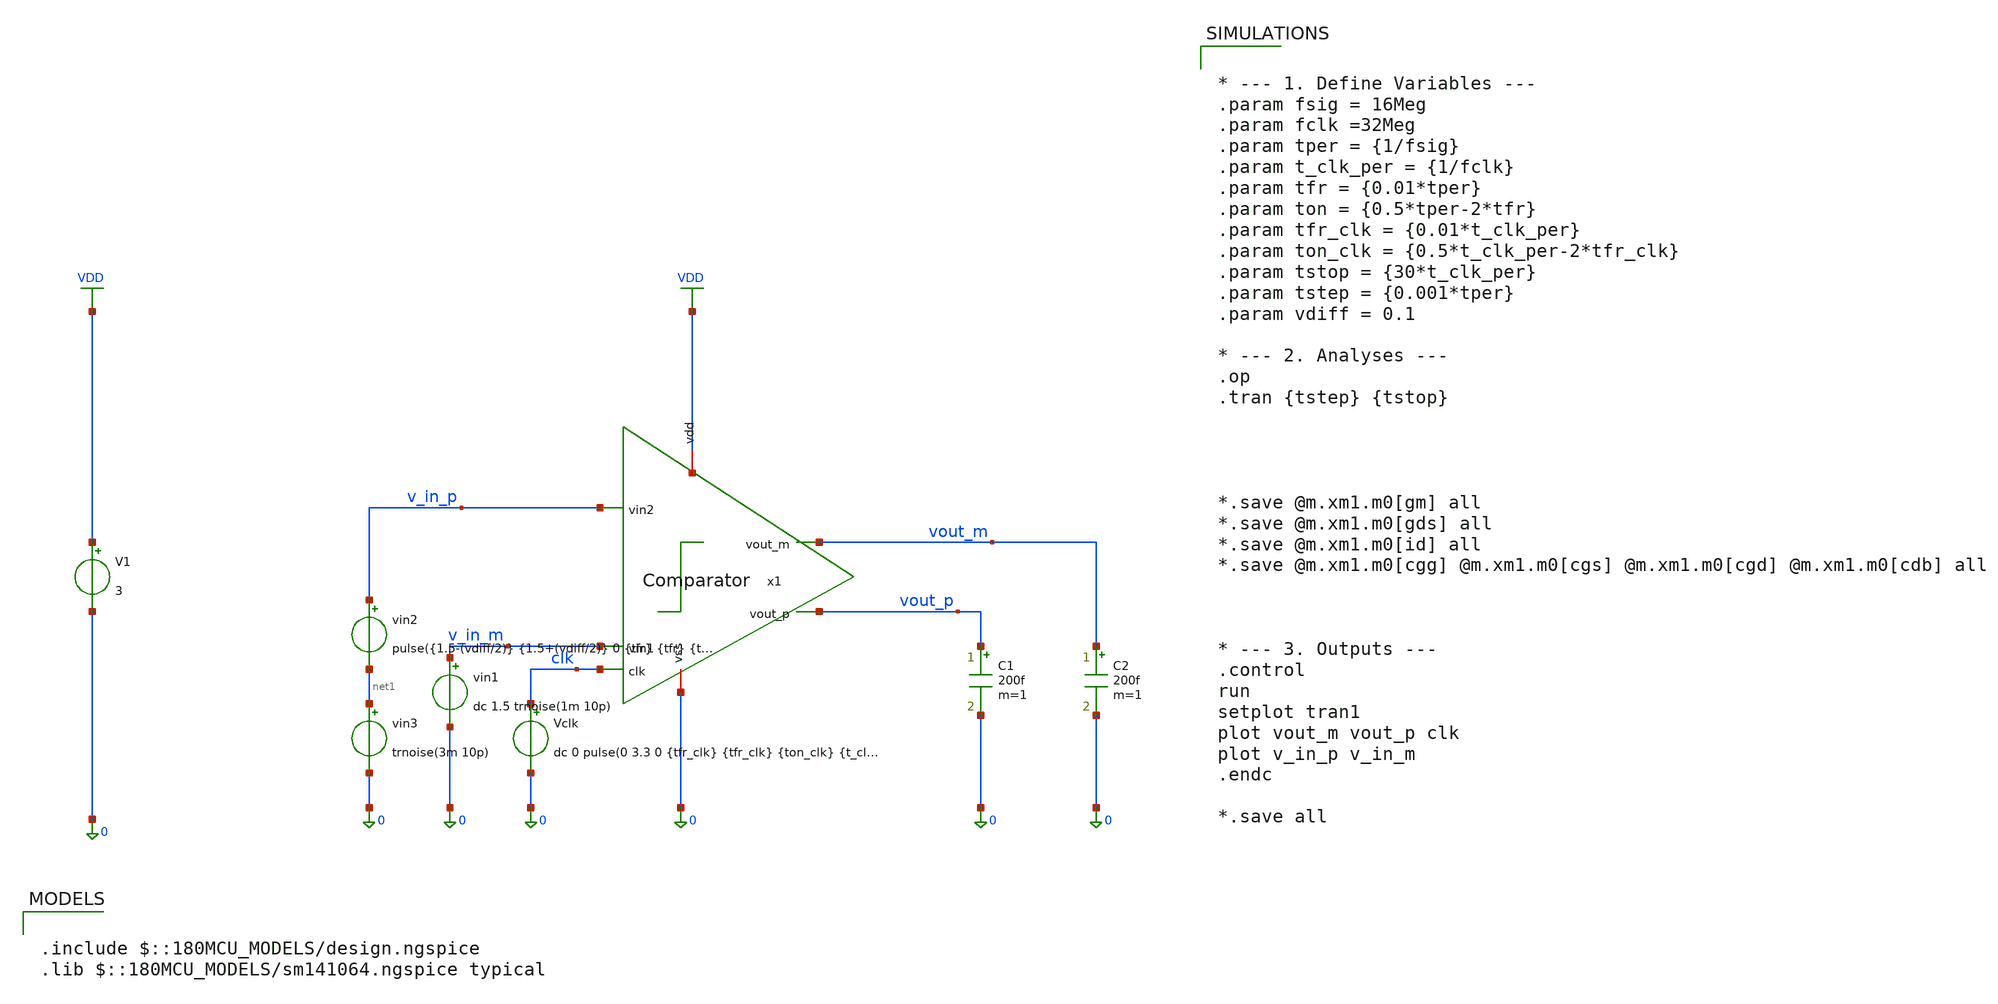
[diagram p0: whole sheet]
** sch_path: Felix/Comparator_tb.sch
**.subckt Comparator_tb
x1 VDD vout_m vout_p v_in_p v_in_m clk 0 Comparator
V1 VDD 0 3
vin2 v_in_p net1 pulse({1.5-(vdiff/2)} {1.5+(vdiff/2)} 0 {tfr} {tfr} {ton} {tper})
vin1 v_in_m 0 dc 1.5 trnoise(1m 10p)
Vclk clk 0 dc 0 pulse(0 3.3 0 {tfr_clk} {tfr_clk} {ton_clk} {t_clk_per})
C1 vout_p 0 200f m=1
C2 vout_m 0 200f m=1
vin3 net1 0 trnoise(3m 10p)
**** begin user architecture code


* --- 1. Define Variables ---
.param fsig = 16Meg
.param fclk =32Meg
.param tper = {1/fsig}
.param t_clk_per = {1/fclk}
.param tfr = {0.01*tper}
.param ton = {0.5*tper-2*tfr}
.param tfr_clk = {0.01*t_clk_per}
.param ton_clk = {0.5*t_clk_per-2*tfr_clk}
.param tstop = {30*t_clk_per}
.param tstep = {0.001*tper}
.param vdiff = 0.1

* --- 2. Analyses ---
.op
.tran {tstep} {tstop}




*.save @m.xm1.m0[gm] all
*.save @m.xm1.m0[gds] all
*.save @m.xm1.m0[id] all
*.save @m.xm1.m0[cgg] @m.xm1.m0[cgs] @m.xm1.m0[cgd] @m.xm1.m0[cdb] all



* --- 3. Outputs ---
.control
run
setplot tran1
plot vout_m vout_p clk
plot v_in_p v_in_m
.endc

*.save all



.include $::180MCU_MODELS/design.ngspice
.lib $::180MCU_MODELS/sm141064.ngspice typical

**** end user architecture code
**.ends

* expanding   symbol:  Comparator.sym # of pins=7
** sym_path: Felix/Comparator.sym
** sch_path: Felix/Comparator.sch
.subckt Comparator vdd vout_m vout_p vin2 vin1 clk vss
*.iopin vdd
*.iopin vss
*.ipin clk
*.ipin vin1
*.ipin vin2
*.opin vout_p
*.opin vout_m
XM1 net1 clk vss vss nfet_03v3 L=1u W=16u nf=1 ad='int((nf+1)/2) * W/nf * 0.18u' as='int((nf+2)/2) * W/nf * 0.18u'
+ pd='2*int((nf+1)/2) * (W/nf + 0.18u)' ps='2*int((nf+2)/2) * (W/nf + 0.18u)' nrd='0.18u / W' nrs='0.18u / W'
+ sa=0 sb=0 sd=0 m=1
XM2 v_diff_p vin1 net1 net1 nfet_03v3 L=1u W=8u nf=1 ad='int((nf+1)/2) * W/nf * 0.18u' as='int((nf+2)/2) * W/nf * 0.18u'
+ pd='2*int((nf+1)/2) * (W/nf + 0.18u)' ps='2*int((nf+2)/2) * (W/nf + 0.18u)' nrd='0.18u / W' nrs='0.18u / W'
+ sa=0 sb=0 sd=0 m=1
XM3 v_diff_m vin2 net1 net1 nfet_03v3 L=1u W=8u nf=1 ad='int((nf+1)/2) * W/nf * 0.18u' as='int((nf+2)/2) * W/nf * 0.18u'
+ pd='2*int((nf+1)/2) * (W/nf + 0.18u)' ps='2*int((nf+2)/2) * (W/nf + 0.18u)' nrd='0.18u / W' nrs='0.18u / W'
+ sa=0 sb=0 sd=0 m=1
XM4 v_out_p_noninv v_out_m_noninv v_diff_p v_diff_p nfet_03v3 L=1u W=8u nf=1 ad='int((nf+1)/2) * W/nf * 0.18u'
+ as='int((nf+2)/2) * W/nf * 0.18u' pd='2*int((nf+1)/2) * (W/nf + 0.18u)' ps='2*int((nf+2)/2) * (W/nf + 0.18u)'
+ nrd='0.18u / W' nrs='0.18u / W' sa=0 sb=0 sd=0 m=1
XM5 v_out_m_noninv v_out_p_noninv v_diff_m v_diff_m nfet_03v3 L=1u W=8u nf=1 ad='int((nf+1)/2) * W/nf * 0.18u'
+ as='int((nf+2)/2) * W/nf * 0.18u' pd='2*int((nf+1)/2) * (W/nf + 0.18u)' ps='2*int((nf+2)/2) * (W/nf + 0.18u)'
+ nrd='0.18u / W' nrs='0.18u / W' sa=0 sb=0 sd=0 m=1
XM6 v_diff_p clk vdd vdd pfet_03v3 L=1u W=4u nf=1 ad='int((nf+1)/2) * W/nf * 0.18u' as='int((nf+2)/2) * W/nf * 0.18u'
+ pd='2*int((nf+1)/2) * (W/nf + 0.18u)' ps='2*int((nf+2)/2) * (W/nf + 0.18u)' nrd='0.18u / W' nrs='0.18u / W'
+ sa=0 sb=0 sd=0 m=1
XM7 v_out_p_noninv clk vdd vdd pfet_03v3 L=1u W=4u nf=1 ad='int((nf+1)/2) * W/nf * 0.18u' as='int((nf+2)/2) * W/nf * 0.18u'
+ pd='2*int((nf+1)/2) * (W/nf + 0.18u)' ps='2*int((nf+2)/2) * (W/nf + 0.18u)' nrd='0.18u / W' nrs='0.18u / W'
+ sa=0 sb=0 sd=0 m=1
XM8 v_out_m_noninv clk vdd vdd pfet_03v3 L=1u W=4u nf=1 ad='int((nf+1)/2) * W/nf * 0.18u' as='int((nf+2)/2) * W/nf * 0.18u'
+ pd='2*int((nf+1)/2) * (W/nf + 0.18u)' ps='2*int((nf+2)/2) * (W/nf + 0.18u)' nrd='0.18u / W' nrs='0.18u / W'
+ sa=0 sb=0 sd=0 m=1
XM9 v_diff_m clk vdd vdd pfet_03v3 L=1u W=4u nf=1 ad='int((nf+1)/2) * W/nf * 0.18u' as='int((nf+2)/2) * W/nf * 0.18u'
+ pd='2*int((nf+1)/2) * (W/nf + 0.18u)' ps='2*int((nf+2)/2) * (W/nf + 0.18u)' nrd='0.18u / W' nrs='0.18u / W'
+ sa=0 sb=0 sd=0 m=1
XM10 v_out_p_noninv v_out_m_noninv vdd vdd pfet_03v3 L=1u W=8u nf=1 ad='int((nf+1)/2) * W/nf * 0.18u'
+ as='int((nf+2)/2) * W/nf * 0.18u' pd='2*int((nf+1)/2) * (W/nf + 0.18u)' ps='2*int((nf+2)/2) * (W/nf + 0.18u)'
+ nrd='0.18u / W' nrs='0.18u / W' sa=0 sb=0 sd=0 m=1
XM11 v_out_m_noninv v_out_p_noninv vdd vdd pfet_03v3 L=1u W=8u nf=1 ad='int((nf+1)/2) * W/nf * 0.18u'
+ as='int((nf+2)/2) * W/nf * 0.18u' pd='2*int((nf+1)/2) * (W/nf + 0.18u)' ps='2*int((nf+2)/2) * (W/nf + 0.18u)'
+ nrd='0.18u / W' nrs='0.18u / W' sa=0 sb=0 sd=0 m=1
XM12 vout_p v_out_m_noninv vss vss nfet_03v3 L=1u W=2u nf=1 ad='int((nf+1)/2) * W/nf * 0.18u' as='int((nf+2)/2) * W/nf * 0.18u'
+ pd='2*int((nf+1)/2) * (W/nf + 0.18u)' ps='2*int((nf+2)/2) * (W/nf + 0.18u)' nrd='0.18u / W' nrs='0.18u / W'
+ sa=0 sb=0 sd=0 m=1
XM13 vout_p v_out_m_noninv vdd vdd pfet_03v3 L=1u W=10u nf=1 ad='int((nf+1)/2) * W/nf * 0.18u' as='int((nf+2)/2) * W/nf * 0.18u'
+ pd='2*int((nf+1)/2) * (W/nf + 0.18u)' ps='2*int((nf+2)/2) * (W/nf + 0.18u)' nrd='0.18u / W' nrs='0.18u / W'
+ sa=0 sb=0 sd=0 m=1
XM14 vout_m v_out_p_noninv vss vss nfet_03v3 L=1u W=2u nf=1 ad='int((nf+1)/2) * W/nf * 0.18u' as='int((nf+2)/2) * W/nf * 0.18u'
+ pd='2*int((nf+1)/2) * (W/nf + 0.18u)' ps='2*int((nf+2)/2) * (W/nf + 0.18u)' nrd='0.18u / W' nrs='0.18u / W'
+ sa=0 sb=0 sd=0 m=1
XM15 vout_m v_out_p_noninv vdd vdd pfet_03v3 L=1u W=10u nf=1 ad='int((nf+1)/2) * W/nf * 0.18u' as='int((nf+2)/2) * W/nf * 0.18u'
+ pd='2*int((nf+1)/2) * (W/nf + 0.18u)' ps='2*int((nf+2)/2) * (W/nf + 0.18u)' nrd='0.18u / W' nrs='0.18u / W'
+ sa=0 sb=0 sd=0 m=1
.ends

.GLOBAL VDD
.end
